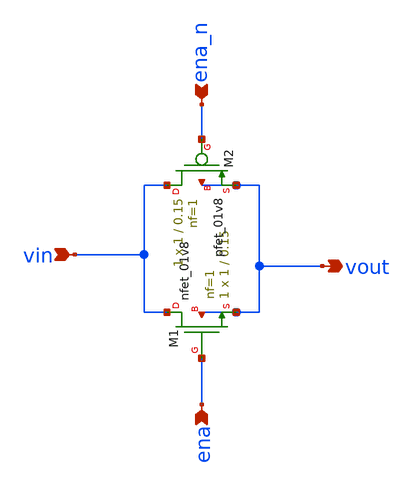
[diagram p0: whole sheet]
** sch_path: xschem/src/output_select/transmission_gate.sch
**.subckt transmission_gate vin vout ena_n ena
*.ipin vin
*.opin vout
*.ipin ena_n
*.ipin ena
XM1 vin ena vout vout sky130_fd_pr__nfet_01v8 L=0.15 W=1 nf=1 ad='int((nf+1)/2) * W/nf * 0.29' as='int((nf+2)/2) * W/nf * 0.29'
+ pd='2*int((nf+1)/2) * (W/nf + 0.29)' ps='2*int((nf+2)/2) * (W/nf + 0.29)' nrd='0.29 / W' nrs='0.29 / W'
+ sa=0 sb=0 sd=0 mult=1 m=1
XM2 vin ena_n vout vout sky130_fd_pr__pfet_01v8 L=0.15 W=1 nf=1 ad='int((nf+1)/2) * W/nf * 0.29' as='int((nf+2)/2) * W/nf * 0.29'
+ pd='2*int((nf+1)/2) * (W/nf + 0.29)' ps='2*int((nf+2)/2) * (W/nf + 0.29)' nrd='0.29 / W' nrs='0.29 / W'
+ sa=0 sb=0 sd=0 mult=1 m=1
**.ends
.end
